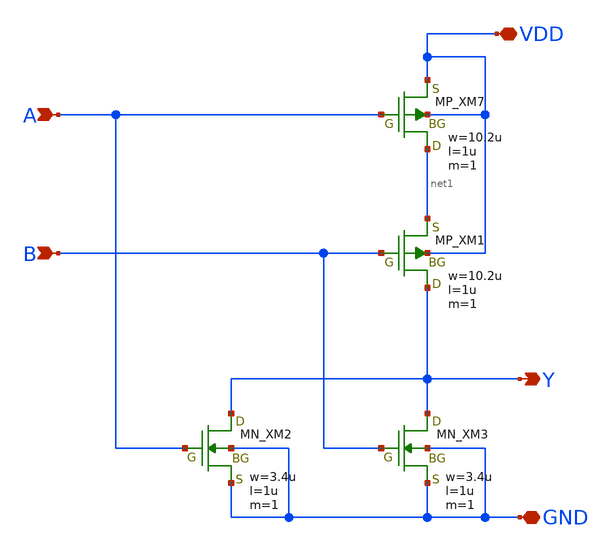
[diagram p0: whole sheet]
** sch_path: openIP62_rev1.0/IP62/Technology/tech/symbols/Xschem/IP62_5_stdcell/NOR2.sch
**.subckt NOR2 A B Y VDD GND
*.ipin A
*.ipin B
*.opin Y
*.iopin VDD
*.iopin GND
XM7 net1 A VDD VDD PMOS w=10.2u l=1u as=0 ad=0 ps=0 pd=0 nrd=0 nrs=0 m=1
XM1 Y B net1 VDD PMOS w=10.2u l=1u as=0 ad=0 ps=0 pd=0 nrd=0 nrs=0 m=1
XM2 Y A GND GND NMOS w=3.4u l=1u as=0 ad=0 ps=0 pd=0 nrd=0 nrs=0 m=1
XM3 Y B GND GND NMOS w=3.4u l=1u as=0 ad=0 ps=0 pd=0 nrd=0 nrs=0 m=1
**.ends
.end
